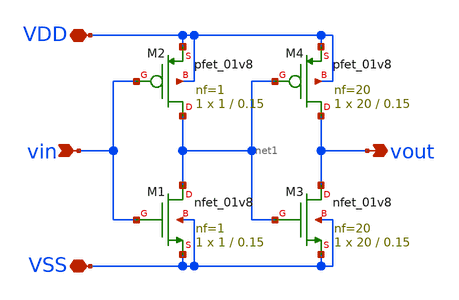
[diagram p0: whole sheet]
** sch_path: xschem/double_inverter.sch
**.subckt double_inverter VDD VSS vin vout
*.iopin VDD
*.iopin VSS
*.ipin vin
*.opin vout
XM1 net1 vin VSS VSS sky130_fd_pr__nfet_01v8 L=0.15 W=1 nf=1 ad='int((nf+1)/2) * W/nf * 0.29' as='int((nf+2)/2) * W/nf * 0.29'
+ pd='2*int((nf+1)/2) * (W/nf + 0.29)' ps='2*int((nf+2)/2) * (W/nf + 0.29)' nrd='0.29 / W' nrs='0.29 / W'
+ sa=0 sb=0 sd=0 mult=1 m=1
XM2 net1 vin VDD VDD sky130_fd_pr__pfet_01v8 L=0.15 W=1 nf=1 ad='int((nf+1)/2) * W/nf * 0.29' as='int((nf+2)/2) * W/nf * 0.29'
+ pd='2*int((nf+1)/2) * (W/nf + 0.29)' ps='2*int((nf+2)/2) * (W/nf + 0.29)' nrd='0.29 / W' nrs='0.29 / W'
+ sa=0 sb=0 sd=0 mult=1 m=1
XM3 vout net1 VSS VSS sky130_fd_pr__nfet_01v8 L=0.15 W=20 nf=20 ad='int((nf+1)/2) * W/nf * 0.29' as='int((nf+2)/2) * W/nf * 0.29'
+ pd='2*int((nf+1)/2) * (W/nf + 0.29)' ps='2*int((nf+2)/2) * (W/nf + 0.29)' nrd='0.29 / W' nrs='0.29 / W'
+ sa=0 sb=0 sd=0 mult=1 m=1
XM4 vout net1 VDD VDD sky130_fd_pr__pfet_01v8 L=0.15 W=20 nf=20 ad='int((nf+1)/2) * W/nf * 0.29' as='int((nf+2)/2) * W/nf * 0.29'
+ pd='2*int((nf+1)/2) * (W/nf + 0.29)' ps='2*int((nf+2)/2) * (W/nf + 0.29)' nrd='0.29 / W' nrs='0.29 / W'
+ sa=0 sb=0 sd=0 mult=1 m=1
**.ends
.end
